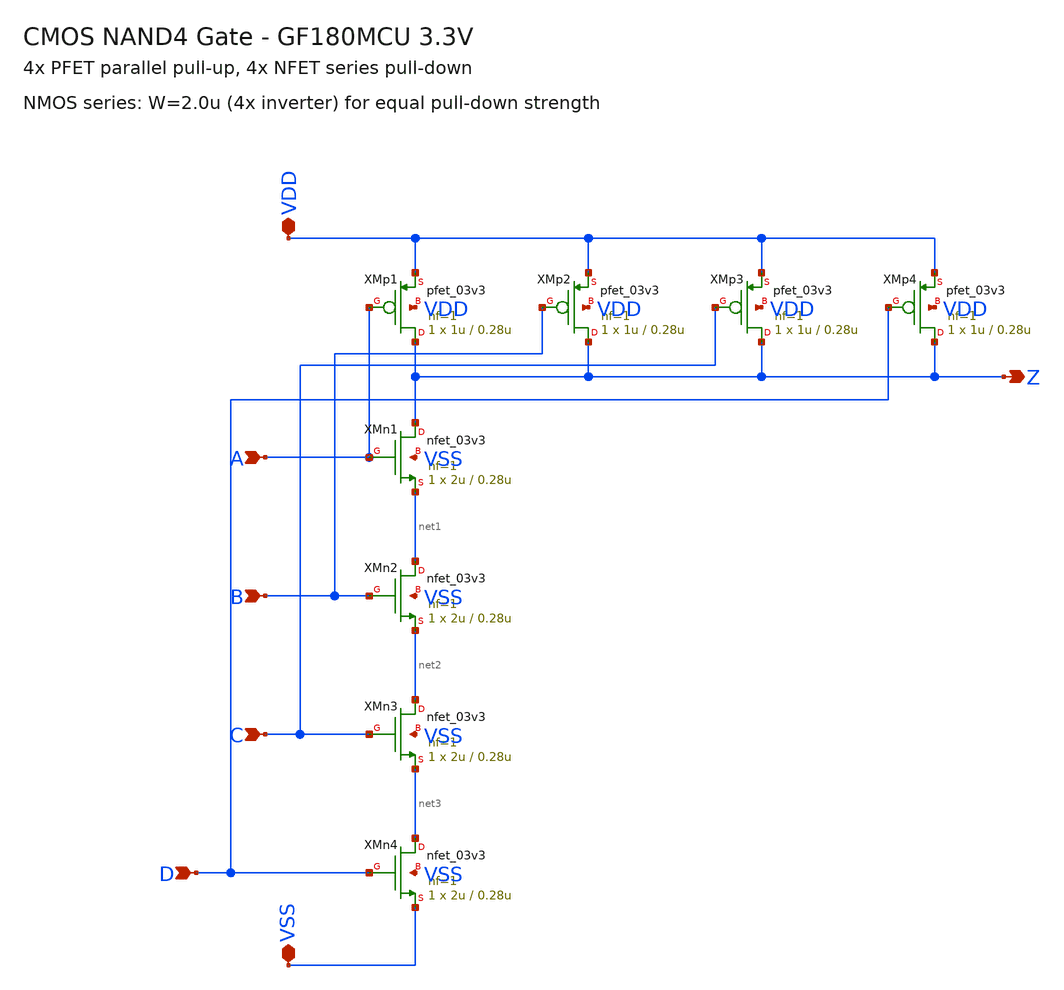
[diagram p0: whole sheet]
** sch_path: designs/libs/core_analog/pfd/nand4_pf.sch
**.subckt nand4_pf VDD VSS A B C D Z
*.iopin VDD
*.iopin VSS
*.ipin A
*.ipin B
*.ipin C
*.ipin D
*.opin Z
XMp1 Z A VDD VDD pfet_03v3 L=0.28u W=1u nf=1 ad='int((nf+1)/2) * W/nf * 0.18u' as='int((nf+2)/2) * W/nf * 0.18u'
+ pd='2*int((nf+1)/2) * (W/nf + 0.18u)' ps='2*int((nf+2)/2) * (W/nf + 0.18u)' nrd='0.18u / W' nrs='0.18u / W'
+ sa=0 sb=0 sd=0 m=1
XMp2 Z B VDD VDD pfet_03v3 L=0.28u W=1u nf=1 ad='int((nf+1)/2) * W/nf * 0.18u' as='int((nf+2)/2) * W/nf * 0.18u'
+ pd='2*int((nf+1)/2) * (W/nf + 0.18u)' ps='2*int((nf+2)/2) * (W/nf + 0.18u)' nrd='0.18u / W' nrs='0.18u / W'
+ sa=0 sb=0 sd=0 m=1
XMp3 Z C VDD VDD pfet_03v3 L=0.28u W=1u nf=1 ad='int((nf+1)/2) * W/nf * 0.18u' as='int((nf+2)/2) * W/nf * 0.18u'
+ pd='2*int((nf+1)/2) * (W/nf + 0.18u)' ps='2*int((nf+2)/2) * (W/nf + 0.18u)' nrd='0.18u / W' nrs='0.18u / W'
+ sa=0 sb=0 sd=0 m=1
XMp4 Z D VDD VDD pfet_03v3 L=0.28u W=1u nf=1 ad='int((nf+1)/2) * W/nf * 0.18u' as='int((nf+2)/2) * W/nf * 0.18u'
+ pd='2*int((nf+1)/2) * (W/nf + 0.18u)' ps='2*int((nf+2)/2) * (W/nf + 0.18u)' nrd='0.18u / W' nrs='0.18u / W'
+ sa=0 sb=0 sd=0 m=1
XMn1 Z A net1 VSS nfet_03v3 L=0.28u W=2u nf=1 ad='int((nf+1)/2) * W/nf * 0.18u' as='int((nf+2)/2) * W/nf * 0.18u'
+ pd='2*int((nf+1)/2) * (W/nf + 0.18u)' ps='2*int((nf+2)/2) * (W/nf + 0.18u)' nrd='0.18u / W' nrs='0.18u / W'
+ sa=0 sb=0 sd=0 m=1
XMn2 net1 B net2 VSS nfet_03v3 L=0.28u W=2u nf=1 ad='int((nf+1)/2) * W/nf * 0.18u' as='int((nf+2)/2) * W/nf * 0.18u'
+ pd='2*int((nf+1)/2) * (W/nf + 0.18u)' ps='2*int((nf+2)/2) * (W/nf + 0.18u)' nrd='0.18u / W' nrs='0.18u / W'
+ sa=0 sb=0 sd=0 m=1
XMn3 net2 C net3 VSS nfet_03v3 L=0.28u W=2u nf=1 ad='int((nf+1)/2) * W/nf * 0.18u' as='int((nf+2)/2) * W/nf * 0.18u'
+ pd='2*int((nf+1)/2) * (W/nf + 0.18u)' ps='2*int((nf+2)/2) * (W/nf + 0.18u)' nrd='0.18u / W' nrs='0.18u / W'
+ sa=0 sb=0 sd=0 m=1
XMn4 net3 D VSS VSS nfet_03v3 L=0.28u W=2u nf=1 ad='int((nf+1)/2) * W/nf * 0.18u' as='int((nf+2)/2) * W/nf * 0.18u'
+ pd='2*int((nf+1)/2) * (W/nf + 0.18u)' ps='2*int((nf+2)/2) * (W/nf + 0.18u)' nrd='0.18u / W' nrs='0.18u / W'
+ sa=0 sb=0 sd=0 m=1
**.ends
.end
